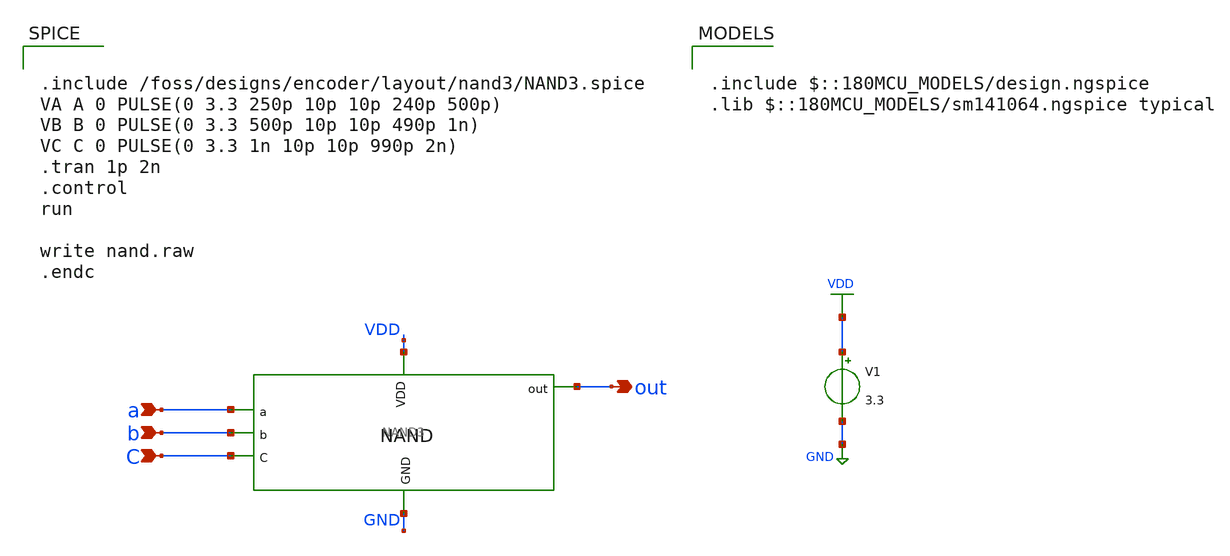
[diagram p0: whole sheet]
** sch_path: blocks/adc/encoder/sym/NAND3_layout_tb.sch
**.subckt NAND3_layout_tb a out C b
*.ipin a
*.opin out
*.ipin C
*.ipin b
V1 VDD GND 3.3
x1 b a VDD out C GND NAND3
**** begin user architecture code


.include /foss/designs/encoder/layout/nand3/NAND3.spice
VA A 0 PULSE(0 3.3 250p 10p 10p 240p 500p)
VB B 0 PULSE(0 3.3 500p 10p 10p 490p 1n)
VC C 0 PULSE(0 3.3 1n 10p 10p 990p 2n)
.tran 1p 2n
.control
run

write nand.raw
.endc



.include $::180MCU_MODELS/design.ngspice
.lib $::180MCU_MODELS/sm141064.ngspice typical

**** end user architecture code
**.ends

* expanding   symbol:  NAND3.sym # of pins=6
** sym_path: blocks/adc/encoder/sym/NAND3.sym
** sch_path: blocks/adc/encoder/sym/NAND3.sch
.subckt NAND3 b a VDD out C GND
*.ipin a
*.opin out
*.ipin C
*.ipin b
*.ipin VDD
*.ipin GND
XM5 out net1 VDD VDD pfet_03v3 L=0.28u W=0.22u nf=1 ad='int((nf+1)/2) * W/nf * 0.18u' as='int((nf+2)/2) * W/nf * 0.18u'
+ pd='2*int((nf+1)/2) * (W/nf + 0.18u)' ps='2*int((nf+2)/2) * (W/nf + 0.18u)' nrd='0.18u / W' nrs='0.18u / W'
+ sa=0 sb=0 sd=0 m=15
XM6 out net1 GND GND nfet_03v3 L=0.28u W=0.22u nf=1 ad='int((nf+1)/2) * W/nf * 0.18u' as='int((nf+2)/2) * W/nf * 0.18u'
+ pd='2*int((nf+1)/2) * (W/nf + 0.18u)' ps='2*int((nf+2)/2) * (W/nf + 0.18u)' nrd='0.18u / W' nrs='0.18u / W'
+ sa=0 sb=0 sd=0 m=7
XM7 cbar C VDD VDD pfet_03v3 L=0.28u W=0.22u nf=1 ad='int((nf+1)/2) * W/nf * 0.18u' as='int((nf+2)/2) * W/nf * 0.18u'
+ pd='2*int((nf+1)/2) * (W/nf + 0.18u)' ps='2*int((nf+2)/2) * (W/nf + 0.18u)' nrd='0.18u / W' nrs='0.18u / W'
+ sa=0 sb=0 sd=0 m=15
XM8 cbar C GND GND nfet_03v3 L=0.28u W=0.22u nf=1 ad='int((nf+1)/2) * W/nf * 0.18u' as='int((nf+2)/2) * W/nf * 0.18u'
+ pd='2*int((nf+1)/2) * (W/nf + 0.18u)' ps='2*int((nf+2)/2) * (W/nf + 0.18u)' nrd='0.18u / W' nrs='0.18u / W'
+ sa=0 sb=0 sd=0 m=7
XM13 net1 a VDD VDD pfet_03v3 L=0.28u W=0.22u nf=1 ad='int((nf+1)/2) * W/nf * 0.18u' as='int((nf+2)/2) * W/nf * 0.18u'
+ pd='2*int((nf+1)/2) * (W/nf + 0.18u)' ps='2*int((nf+2)/2) * (W/nf + 0.18u)' nrd='0.18u / W' nrs='0.18u / W'
+ sa=0 sb=0 sd=0 m=15
XM14 net1 b VDD VDD pfet_03v3 L=0.28u W=0.22u nf=1 ad='int((nf+1)/2) * W/nf * 0.18u' as='int((nf+2)/2) * W/nf * 0.18u'
+ pd='2*int((nf+1)/2) * (W/nf + 0.18u)' ps='2*int((nf+2)/2) * (W/nf + 0.18u)' nrd='0.18u / W' nrs='0.18u / W'
+ sa=0 sb=0 sd=0 m=15
XM15 net1 cbar VDD VDD pfet_03v3 L=0.28u W=0.22u nf=1 ad='int((nf+1)/2) * W/nf * 0.18u' as='int((nf+2)/2) * W/nf * 0.18u'
+ pd='2*int((nf+1)/2) * (W/nf + 0.18u)' ps='2*int((nf+2)/2) * (W/nf + 0.18u)' nrd='0.18u / W' nrs='0.18u / W'
+ sa=0 sb=0 sd=0 m=15
XM16 net1 a net2 GND nfet_03v3 L=0.28u W=0.22u nf=1 ad='int((nf+1)/2) * W/nf * 0.18u' as='int((nf+2)/2) * W/nf * 0.18u'
+ pd='2*int((nf+1)/2) * (W/nf + 0.18u)' ps='2*int((nf+2)/2) * (W/nf + 0.18u)' nrd='0.18u / W' nrs='0.18u / W'
+ sa=0 sb=0 sd=0 m=7
XM17 net2 b net3 GND nfet_03v3 L=0.28u W=0.22u nf=1 ad='int((nf+1)/2) * W/nf * 0.18u' as='int((nf+2)/2) * W/nf * 0.18u'
+ pd='2*int((nf+1)/2) * (W/nf + 0.18u)' ps='2*int((nf+2)/2) * (W/nf + 0.18u)' nrd='0.18u / W' nrs='0.18u / W'
+ sa=0 sb=0 sd=0 m=7
XM18 net3 cbar GND GND nfet_03v3 L=0.28u W=0.22u nf=1 ad='int((nf+1)/2) * W/nf * 0.18u' as='int((nf+2)/2) * W/nf * 0.18u'
+ pd='2*int((nf+1)/2) * (W/nf + 0.18u)' ps='2*int((nf+2)/2) * (W/nf + 0.18u)' nrd='0.18u / W' nrs='0.18u / W'
+ sa=0 sb=0 sd=0 m=7
.ends

.GLOBAL VDD
.GLOBAL GND
.end
